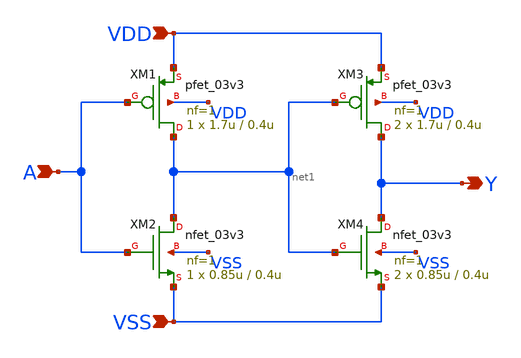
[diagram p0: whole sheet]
** sch_path: designs/comparator/final_magic/osu_sc/mybuffer/buffer2x.sch
**.subckt buffer2x A Y VDD VSS
*.ipin A
*.opin Y
*.ipin VDD
*.ipin VSS
XM1 net1 A VDD VDD pfet_03v3 L=0.4u W=1.7u nf=1 ad='int((nf+1)/2) * W/nf * 0.18u' as='int((nf+2)/2) * W/nf * 0.18u'
+ pd='2*int((nf+1)/2) * (W/nf + 0.18u)' ps='2*int((nf+2)/2) * (W/nf + 0.18u)' nrd='0.18u / W' nrs='0.18u / W'
+ sa=0 sb=0 sd=0 m=1
XM2 net1 A VSS VSS nfet_03v3 L=0.4u W=0.85u nf=1 ad='int((nf+1)/2) * W/nf * 0.18u' as='int((nf+2)/2) * W/nf * 0.18u'
+ pd='2*int((nf+1)/2) * (W/nf + 0.18u)' ps='2*int((nf+2)/2) * (W/nf + 0.18u)' nrd='0.18u / W' nrs='0.18u / W'
+ sa=0 sb=0 sd=0 m=1
XM3 Y net1 VDD VDD pfet_03v3 L=0.4u W=1.7u nf=1 ad='int((nf+1)/2) * W/nf * 0.18u' as='int((nf+2)/2) * W/nf * 0.18u'
+ pd='2*int((nf+1)/2) * (W/nf + 0.18u)' ps='2*int((nf+2)/2) * (W/nf + 0.18u)' nrd='0.18u / W' nrs='0.18u / W'
+ sa=0 sb=0 sd=0 m=2
XM4 Y net1 VSS VSS nfet_03v3 L=0.4u W=0.85u nf=1 ad='int((nf+1)/2) * W/nf * 0.18u' as='int((nf+2)/2) * W/nf * 0.18u'
+ pd='2*int((nf+1)/2) * (W/nf + 0.18u)' ps='2*int((nf+2)/2) * (W/nf + 0.18u)' nrd='0.18u / W' nrs='0.18u / W'
+ sa=0 sb=0 sd=0 m=2
**.ends
.end
